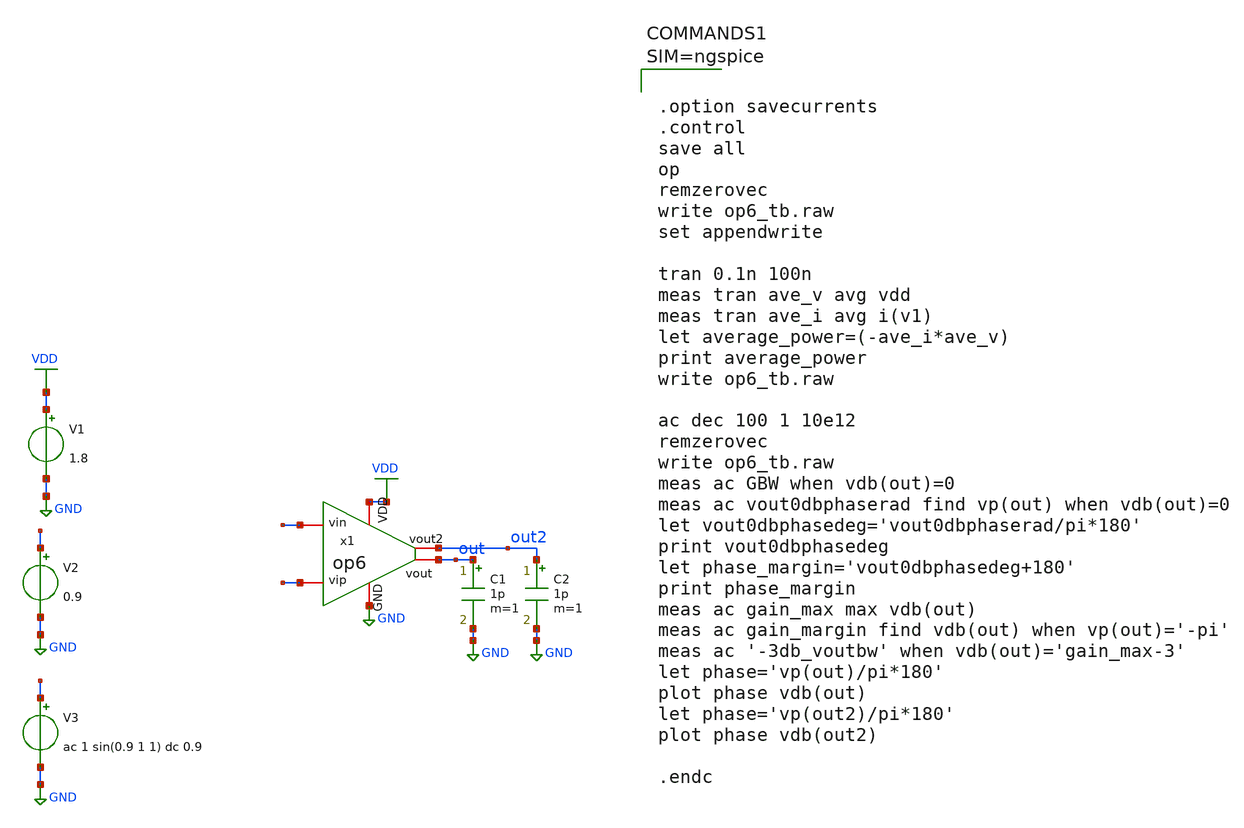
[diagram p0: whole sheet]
** sch_path: xschem/op6_tb.sch
**.subckt op6_tb
V1 VDD GND 1.8
V2 - GND 0.9
V3 + GND ac 1 sin(0.9 1 1) dc 0.9
C1 out GND 1p m=1
x1 VDD - + out2 out GND op6
C2 out2 GND 1p m=1
**** begin user architecture code

** opencircuitdesign pdks install
.lib $::SKYWATER_MODELS/sky130.lib.spice tt





.option savecurrents
.control
save all
op
remzerovec
write op6_tb.raw
set appendwrite

tran 0.1n 100n
meas tran ave_v avg vdd
meas tran ave_i avg i(v1)
let average_power=(-ave_i*ave_v)
print average_power
write op6_tb.raw

ac dec 100 1 10e12
remzerovec
write op6_tb.raw
meas ac GBW when vdb(out)=0
meas ac vout0dbphaserad find vp(out) when vdb(out)=0
let vout0dbphasedeg='vout0dbphaserad/pi*180'
print vout0dbphasedeg
let phase_margin='vout0dbphasedeg+180'
print phase_margin
meas ac gain_max max vdb(out)
meas ac gain_margin find vdb(out) when vp(out)='-pi'
meas ac '-3db_voutbw' when vdb(out)='gain_max-3'
let phase='vp(out)/pi*180'
plot phase vdb(out)
let phase='vp(out2)/pi*180'
plot phase vdb(out2)

.endc



**** end user architecture code
**.ends

* expanding   symbol:  op6.sym # of pins=6
** sym_path: xschem/op6.sym
** sch_path: xschem/op6.sch
.subckt op6 VDD vin vip vout2 vout GND
*.iopin VDD
*.iopin GND
*.iopin vout
*.iopin vip
*.iopin vin
*.iopin vout2
XM1 net1 net1 VDD VDD sky130_fd_pr__pfet_01v8 L={L1} W={W1} nf=1 ad='int((nf+1)/2) * W/nf * 0.29' as='int((nf+2)/2) * W/nf * 0.29'
+ pd='2*int((nf+1)/2) * (W/nf + 0.29)' ps='2*int((nf+2)/2) * (W/nf + 0.29)' nrd='0.29 / W' nrs='0.29 / W'
+ sa=0 sb=0 sd=0 mult={M1} m={M1}
XM2 net2 net2 net1 VDD sky130_fd_pr__pfet_01v8 L={L1} W={W1} nf=1 ad='int((nf+1)/2) * W/nf * 0.29' as='int((nf+2)/2) * W/nf * 0.29'
+ pd='2*int((nf+1)/2) * (W/nf + 0.29)' ps='2*int((nf+2)/2) * (W/nf + 0.29)' nrd='0.29 / W' nrs='0.29 / W'
+ sa=0 sb=0 sd=0 mult={M1} m={M1}
XM3 net4 net1 VDD VDD sky130_fd_pr__pfet_01v8 L={L6} W={W6} nf=1 ad='int((nf+1)/2) * W/nf * 0.29' as='int((nf+2)/2) * W/nf * 0.29'
+ pd='2*int((nf+1)/2) * (W/nf + 0.29)' ps='2*int((nf+2)/2) * (W/nf + 0.29)' nrd='0.29 / W' nrs='0.29 / W'
+ sa=0 sb=0 sd=0 mult={M6} m={M6}
XM4 net3 net2 net4 VDD sky130_fd_pr__pfet_01v8 L={L6} W={W6} nf=1 ad='int((nf+1)/2) * W/nf * 0.29' as='int((nf+2)/2) * W/nf * 0.29'
+ pd='2*int((nf+1)/2) * (W/nf + 0.29)' ps='2*int((nf+2)/2) * (W/nf + 0.29)' nrd='0.29 / W' nrs='0.29 / W'
+ sa=0 sb=0 sd=0 mult={M6} m={M6}
XM5 net5 net1 VDD VDD sky130_fd_pr__pfet_01v8 L={L5} W={W5} nf=1 ad='int((nf+1)/2) * W/nf * 0.29' as='int((nf+2)/2) * W/nf * 0.29'
+ pd='2*int((nf+1)/2) * (W/nf + 0.29)' ps='2*int((nf+2)/2) * (W/nf + 0.29)' nrd='0.29 / W' nrs='0.29 / W'
+ sa=0 sb=0 sd=0 mult={M5} m={M5}
XM6 vout2 net2 net5 VDD sky130_fd_pr__pfet_01v8 L={L5} W={W5} nf=1 ad='int((nf+1)/2) * W/nf * 0.29' as='int((nf+2)/2) * W/nf * 0.29'
+ pd='2*int((nf+1)/2) * (W/nf + 0.29)' ps='2*int((nf+2)/2) * (W/nf + 0.29)' nrd='0.29 / W' nrs='0.29 / W'
+ sa=0 sb=0 sd=0 mult={M5} m={M5}
XM7 net6 vin net3 VDD sky130_fd_pr__pfet_01v8 L={L2} W={W2} nf=1 ad='int((nf+1)/2) * W/nf * 0.29' as='int((nf+2)/2) * W/nf * 0.29'
+ pd='2*int((nf+1)/2) * (W/nf + 0.29)' ps='2*int((nf+2)/2) * (W/nf + 0.29)' nrd='0.29 / W' nrs='0.29 / W'
+ sa=0 sb=0 sd=0 mult={M2} m={M2}
XM8 vout vip net3 VDD sky130_fd_pr__pfet_01v8 L={L2} W={W2} nf=1 ad='int((nf+1)/2) * W/nf * 0.29' as='int((nf+2)/2) * W/nf * 0.29'
+ pd='2*int((nf+1)/2) * (W/nf + 0.29)' ps='2*int((nf+2)/2) * (W/nf + 0.29)' nrd='0.29 / W' nrs='0.29 / W'
+ sa=0 sb=0 sd=0 mult={M2} m={M2}
XM9 vout net6 GND GND sky130_fd_pr__nfet_01v8 L={L3} W={W3} nf=1 ad='int((nf+1)/2) * W/nf * 0.29' as='int((nf+2)/2) * W/nf * 0.29'
+ pd='2*int((nf+1)/2) * (W/nf + 0.29)' ps='2*int((nf+2)/2) * (W/nf + 0.29)' nrd='0.29 / W' nrs='0.29 / W'
+ sa=0 sb=0 sd=0 mult={M3} m={M3}
XM10 net6 net6 GND GND sky130_fd_pr__nfet_01v8 L={L3} W={W3} nf=1 ad='int((nf+1)/2) * W/nf * 0.29' as='int((nf+2)/2) * W/nf * 0.29'
+ pd='2*int((nf+1)/2) * (W/nf + 0.29)' ps='2*int((nf+2)/2) * (W/nf + 0.29)' nrd='0.29 / W' nrs='0.29 / W'
+ sa=0 sb=0 sd=0 mult={M3} m={M3}
XM11 vout2 vout GND GND sky130_fd_pr__nfet_01v8 L={L4} W={W4} nf=1 ad='int((nf+1)/2) * W/nf * 0.29' as='int((nf+2)/2) * W/nf * 0.29'
+ pd='2*int((nf+1)/2) * (W/nf + 0.29)' ps='2*int((nf+2)/2) * (W/nf + 0.29)' nrd='0.29 / W' nrs='0.29 / W'
+ sa=0 sb=0 sd=0 mult={M4} m={M4}
XM12 net2 net8 GND GND sky130_fd_pr__nfet_01v8 L={L7} W={W7} nf=1 ad='int((nf+1)/2) * W/nf * 0.29' as='int((nf+2)/2) * W/nf * 0.29'
+ pd='2*int((nf+1)/2) * (W/nf + 0.29)' ps='2*int((nf+2)/2) * (W/nf + 0.29)' nrd='0.29 / W' nrs='0.29 / W'
+ sa=0 sb=0 sd=0 mult={M7} m={M7}
C1 vout2 net7 1p m=1
R1 net7 vout 1k m=1
**** begin user architecture code


***PMOS***
.param L1=1
.param W1=1
.param M1=4

***NMOS current source***
.param L7=1
.param W7=10
.param M7=4

***Diffpair***
.param L2=2.5
.param W2=35
.param M2=4

***NMOS load***
.param L3=2
.param W3=15
.param M3=4

***NMOS second stage***
.param L4=5
.param W4=30
.param M4=4

***PMOS current source second***
.param L5=0.4
.param W5=7
.param M5=4

***PMOS current source***
.param L6=0.4
.param W6=7
.param M6=4


**** end user architecture code
V1 net8 GND 0.6
.ends

.GLOBAL VDD
.GLOBAL GND
.end
